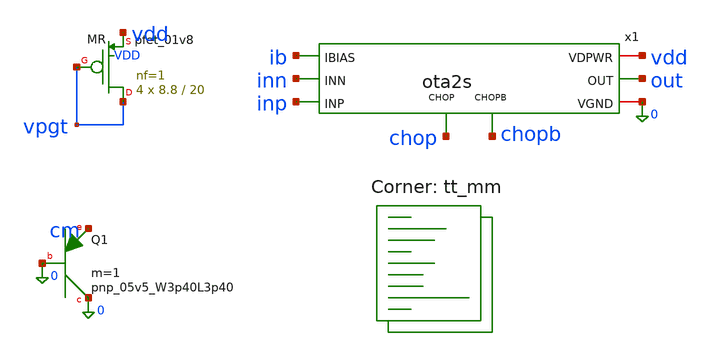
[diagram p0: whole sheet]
** sch_path: xschem/tb_m3_olmc.sch
**.subckt tb_m3_olmc
x1 inp inn out vdd 0 ib chop chopb ota2s
XMR vpgt vpgt vdd VDD sky130_fd_pr__pfet_01v8 L=20 W=8.8 nf=1 ad='int((1 + 1)/2) * 8.8 / 1 * 0.29' as='int((1 + 2)/2) * 8.8 / 1 * 0.29'
+ pd='2*int((1 + 1)/2) * (8.8 / 1 + 0.29)' ps='2*int((1 + 2)/2) * (8.8 / 1 + 0.29)' nrd='0.29 / 8.8 ' nrs='0.29 / 8.8 '
+ sa=0 sb=0 sd=0 mult=4 m=4
XQ1 0 0 cm sky130_fd_pr__pnp_05v5_W3p40L3p40 m=1
**** begin user architecture code
.lib $::SKYWATER_MODELS/sky130.lib.spice tt_mm

.param vdd=1.8 rs=1
Vdd vdd 0 {vdd}
* door 1: input CM = real diode PNP at I_PTAT(T) (rs = R1 corner, denominator = R1 tempco)
Bcm vdd cm I = 2.79e-6*rs*(temper+273.15)/298.15/(1+4.89e-4*(temper-27)+1.2e-6*(temper-27)**2)
* door 2: PTAT bias, I_PTAT/2, sunk from IBIAS
Bib ib 0 I = 1.40e-6*rs*(temper+273.15)/298.15/(1+4.89e-4*(temper-27)+1.2e-6*(temper-27)**2)
* door 4: replica P1 -> vpg target
Brp vpgt 0 I = 2.79e-6*rs*(temper+273.15)/298.15/(1+4.89e-4*(temper-27)+1.2e-6*(temper-27)**2)
* chop state A
Vchop chop 0 0
Vchopb chopb 0 {vdd}
* AC test signal on INP, through the core's node-B impedance
Vac sa cm dc 0 ac 1
RsB sa inp 28.7k
* servo: closed at DC (Lsv shorts), open at AC (Lsv opens, Csv grounds s)
Lsv out s 1T
Csv s 0 1T
Bsv sn cm V = 0.5*tanh(2000*(v(s)-v(vpgt)))
RsA sn inn 9.2k
* the PMOS gate line the op-amp drives in the bandgap
CL out 0 16p
.control
setseed 44
let nmax = 200
let a0v = vector(nmax)
let f44v = vector(nmax)
let pm44v = vector(nmax)
let n = 0
while n < nmax
  reset
  option temp=25
  alter cl = 25p
  ac dec 10 0.01 100meg
  let gdb = vdb(out)
  let phd = cph(v(out))*180/pi
  meas ac a0 find gdb at=0.1
  meas ac f44 when gdb=7.131
  meas ac ph44 find phd at=$&f44
  let a0v[n] = a0
  let f44v[n] = f44/1000
  let pm44v[n] = 180+ph44
  let n = n + 1
end
setplot const
let a0m = mean(a0v)
let a0s = sqrt(mean((a0v-a0m)^2)*nmax/(nmax-1))
let a0min = vecmin(a0v)
let pmm = mean(pm44v)
let pms = sqrt(mean((pm44v-pmm)^2)*nmax/(nmax-1))
let pmmin = vecmin(pm44v)
let fmin = vecmin(f44v)
let fmax = vecmax(f44v)
echo OLMC corner=tt_mm seed=44 N=$&nmax a0_mean_dB=$&a0m a0_sigma_dB=$&a0s a0_min_dB=$&a0min pm44_mean=$&pmm pm44_sigma=$&pms pm44_min=$&pmmin f44_min_kHz=$&fmin f44_max_kHz=$&fmax
let sample = vector(nmax)
setscale sample
wrdata olmc_tt_mm_44.csv a0v f44v pm44v
.endc

**** end user architecture code
**.ends

* expanding   symbol:  ota2s.sym # of pins=8
** sym_path: xschem/ota2s.sym
** sch_path: xschem/ota2s.sch
.subckt ota2s INP INN OUT VDPWR VGND IBIAS CHOP CHOPB
*.ipin INN
*.ipin INP
*.ipin IBIAS
*.opin OUT
*.iopin VDPWR
*.iopin VGND
*.ipin CHOPB
*.ipin CHOP
XMREF IBIAS IBIAS VDPWR VDPWR sky130_fd_pr__pfet_01v8 L=4 W=20 nf=1 ad='int((1 + 1)/2) * 20 / 1 * 0.29' as='int((1
+ + 2)/2) * 20 / 1 * 0.29' pd='2*int((1 + 1)/2) * (20 / 1 + 0.29)' ps='2*int((1 + 2)/2) * (20 / 1 + 0.29)' nrd='0.29
+ / 20 ' nrs='0.29 / 20 ' sa=0 sb=0 sd=0 mult=1 m=1
XMTAIL tail IBIAS VDPWR VDPWR sky130_fd_pr__pfet_01v8 L=4 W=20 nf=1 ad='int((1 + 1)/2) * 20 / 1 * 0.29' as='int((1
+ + 2)/2) * 20 / 1 * 0.29' pd='2*int((1 + 1)/2) * (20 / 1 + 0.29)' ps='2*int((1 + 2)/2) * (20 / 1 + 0.29)' nrd='0.29
+ / 20 ' nrs='0.29 / 20 ' sa=0 sb=0 sd=0 mult=2 m=2
XMP1 d1 INN tail VDPWR sky130_fd_pr__pfet_01v8_lvt L=6 W=25 nf=1 ad='int((1 + 1)/2) * 25 / 1 * 0.29' as='int((1
+ + 2)/2) * 25 / 1 * 0.29' pd='2*int((1 + 1)/2) * (25 / 1 + 0.29)' ps='2*int((1 + 2)/2) * (25 / 1 + 0.29)' nrd='0.29
+ / 25 ' nrs='0.29 / 25 ' sa=0 sb=0 sd=0 mult=24 m=24
XMP2 x1 INP tail VDPWR sky130_fd_pr__pfet_01v8_lvt L=6 W=25 nf=1 ad='int((1 + 1)/2) * 25 / 1 * 0.29' as='int((1
+ + 2)/2) * 25 / 1 * 0.29' pd='2*int((1 + 1)/2) * (25 / 1 + 0.29)' ps='2*int((1 + 2)/2) * (25 / 1 + 0.29)' nrd='0.29
+ / 25 ' nrs='0.29 / 25 ' sa=0 sb=0 sd=0 mult=24 m=24
XMN1 d1 g12 VGND VGND sky130_fd_pr__nfet_01v8 L=20 W=6 nf=1 ad='int((1 + 1)/2) * 6 / 1 * 0.29' as='int((1
+ + 2)/2) * 6 / 1 * 0.29' pd='2*int((1 + 1)/2) * (6 / 1 + 0.29)' ps='2*int((1 + 2)/2) * (6 / 1 + 0.29)' nrd='0.29
+ / 6 ' nrs='0.29 / 6 ' sa=0 sb=0 sd=0 mult=2 m=2
XMN2 x1 g12 VGND VGND sky130_fd_pr__nfet_01v8 L=20 W=6 nf=1 ad='int((1 + 1)/2) * 6 / 1 * 0.29' as='int((1
+ + 2)/2) * 6 / 1 * 0.29' pd='2*int((1 + 1)/2) * (6 / 1 + 0.29)' ps='2*int((1 + 2)/2) * (6 / 1 + 0.29)' nrd='0.29
+ / 6 ' nrs='0.29 / 6 ' sa=0 sb=0 sd=0 mult=2 m=2
XMP3 OUT IBIAS VDPWR VDPWR sky130_fd_pr__pfet_01v8 L=4 W=20 nf=1 ad='int((1 + 1)/2) * 20 / 1 * 0.29' as='int((1
+ + 2)/2) * 20 / 1 * 0.29' pd='2*int((1 + 1)/2) * (20 / 1 + 0.29)' ps='2*int((1 + 2)/2) * (20 / 1 + 0.29)' nrd='0.29
+ / 20 ' nrs='0.29 / 20 ' sa=0 sb=0 sd=0 mult=6 m=6
XMN3 OUT g3 VGND VGND sky130_fd_pr__nfet_01v8 L=1 W=7 nf=1 ad='int((1 + 1)/2) * 7 / 1 * 0.29' as='int((1
+ + 2)/2) * 7 / 1 * 0.29' pd='2*int((1 + 1)/2) * (7 / 1 + 0.29)' ps='2*int((1 + 2)/2) * (7 / 1 + 0.29)' nrd='0.29
+ / 7 ' nrs='0.29 / 7 ' sa=0 sb=0 sd=0 mult=1 m=1
XRZ1 net1 g3 VGND sky130_fd_pr__res_high_po_1p41 L=20 mult=1 m=1
XRZ2 net2 net1 VGND sky130_fd_pr__res_high_po_1p41 L=20 mult=1 m=1
XRZ3 net3 net2 VGND sky130_fd_pr__res_high_po_1p41 L=20 mult=1 m=1
XRZ4 net4 net3 VGND sky130_fd_pr__res_high_po_1p41 L=20 mult=1 m=1
XRZ5 net5 net4 VGND sky130_fd_pr__res_high_po_1p41 L=20 mult=1 m=1
XRZ6 cz net5 VGND sky130_fd_pr__res_high_po_1p41 L=20 mult=1 m=1
XCC cz OUT sky130_fd_pr__cap_mim_m3_1 W=25 L=25 MF=8 m=8
XDP tail VDPWR tail VDPWR sky130_fd_pr__pfet_01v8_lvt L=6 W=25 nf=1 ad='int((1 + 1)/2) * 25 / 1 * 0.29' as='int((1
+ + 2)/2) * 25 / 1 * 0.29' pd='2*int((1 + 1)/2) * (25 / 1 + 0.29)' ps='2*int((1 + 2)/2) * (25 / 1 + 0.29)' nrd='0.29
+ / 25 ' nrs='0.29 / 25 ' sa=0 sb=0 sd=0 mult=8 m=8
XDNA d1 VGND VGND VGND sky130_fd_pr__nfet_01v8 L=20 W=6 nf=1 ad='int((1 + 1)/2) * 6 / 1 * 0.29' as='int((1
+ + 2)/2) * 6 / 1 * 0.29' pd='2*int((1 + 1)/2) * (6 / 1 + 0.29)' ps='2*int((1 + 2)/2) * (6 / 1 + 0.29)' nrd='0.29
+ / 6 ' nrs='0.29 / 6 ' sa=0 sb=0 sd=0 mult=2 m=2
XDNB x1 VGND VGND VGND sky130_fd_pr__nfet_01v8 L=20 W=6 nf=1 ad='int((1 + 1)/2) * 6 / 1 * 0.29' as='int((1
+ + 2)/2) * 6 / 1 * 0.29' pd='2*int((1 + 1)/2) * (6 / 1 + 0.29)' ps='2*int((1 + 2)/2) * (6 / 1 + 0.29)' nrd='0.29
+ / 6 ' nrs='0.29 / 6 ' sa=0 sb=0 sd=0 mult=2 m=2
XDB VDPWR VDPWR VDPWR VDPWR sky130_fd_pr__pfet_01v8 L=4 W=20 nf=1 ad='int((1 + 1)/2) * 20 / 1 * 0.29' as='int((1
+ + 2)/2) * 20 / 1 * 0.29' pd='2*int((1 + 1)/2) * (20 / 1 + 0.29)' ps='2*int((1 + 2)/2) * (20 / 1 + 0.29)' nrd='0.29
+ / 20 ' nrs='0.29 / 20 ' sa=0 sb=0 sd=0 mult=2 m=2
XRD1 VGND VGND VGND sky130_fd_pr__res_high_po_1p41 L=20 mult=1 m=1
XRD2 VGND VGND VGND sky130_fd_pr__res_high_po_1p41 L=20 mult=1 m=1
XSD1 d1 CHOPB g12 VGND sky130_fd_pr__nfet_01v8 L=0.5 W=6 nf=1 ad='int((1 + 1)/2) * 6 / 1 * 0.29' as='int((1
+ + 2)/2) * 6 / 1 * 0.29' pd='2*int((1 + 1)/2) * (6 / 1 + 0.29)' ps='2*int((1 + 2)/2) * (6 / 1 + 0.29)' nrd='0.29
+ / 6 ' nrs='0.29 / 6 ' sa=0 sb=0 sd=0 mult=1 m=1
XSD2 x1 CHOP g12 VGND sky130_fd_pr__nfet_01v8 L=0.5 W=6 nf=1 ad='int((1 + 1)/2) * 6 / 1 * 0.29' as='int((1
+ + 2)/2) * 6 / 1 * 0.29' pd='2*int((1 + 1)/2) * (6 / 1 + 0.29)' ps='2*int((1 + 2)/2) * (6 / 1 + 0.29)' nrd='0.29
+ / 6 ' nrs='0.29 / 6 ' sa=0 sb=0 sd=0 mult=1 m=1
XSG2 g3 CHOP d1 VGND sky130_fd_pr__nfet_01v8 L=0.5 W=6 nf=1 ad='int((1 + 1)/2) * 6 / 1 * 0.29' as='int((1
+ + 2)/2) * 6 / 1 * 0.29' pd='2*int((1 + 1)/2) * (6 / 1 + 0.29)' ps='2*int((1 + 2)/2) * (6 / 1 + 0.29)' nrd='0.29
+ / 6 ' nrs='0.29 / 6 ' sa=0 sb=0 sd=0 mult=1 m=1
XSG1 x1 CHOPB g3 VGND sky130_fd_pr__nfet_01v8 L=0.5 W=6 nf=1 ad='int((1 + 1)/2) * 6 / 1 * 0.29' as='int((1
+ + 2)/2) * 6 / 1 * 0.29' pd='2*int((1 + 1)/2) * (6 / 1 + 0.29)' ps='2*int((1 + 2)/2) * (6 / 1 + 0.29)' nrd='0.29
+ / 6 ' nrs='0.29 / 6 ' sa=0 sb=0 sd=0 mult=1 m=1
.ends

.end
